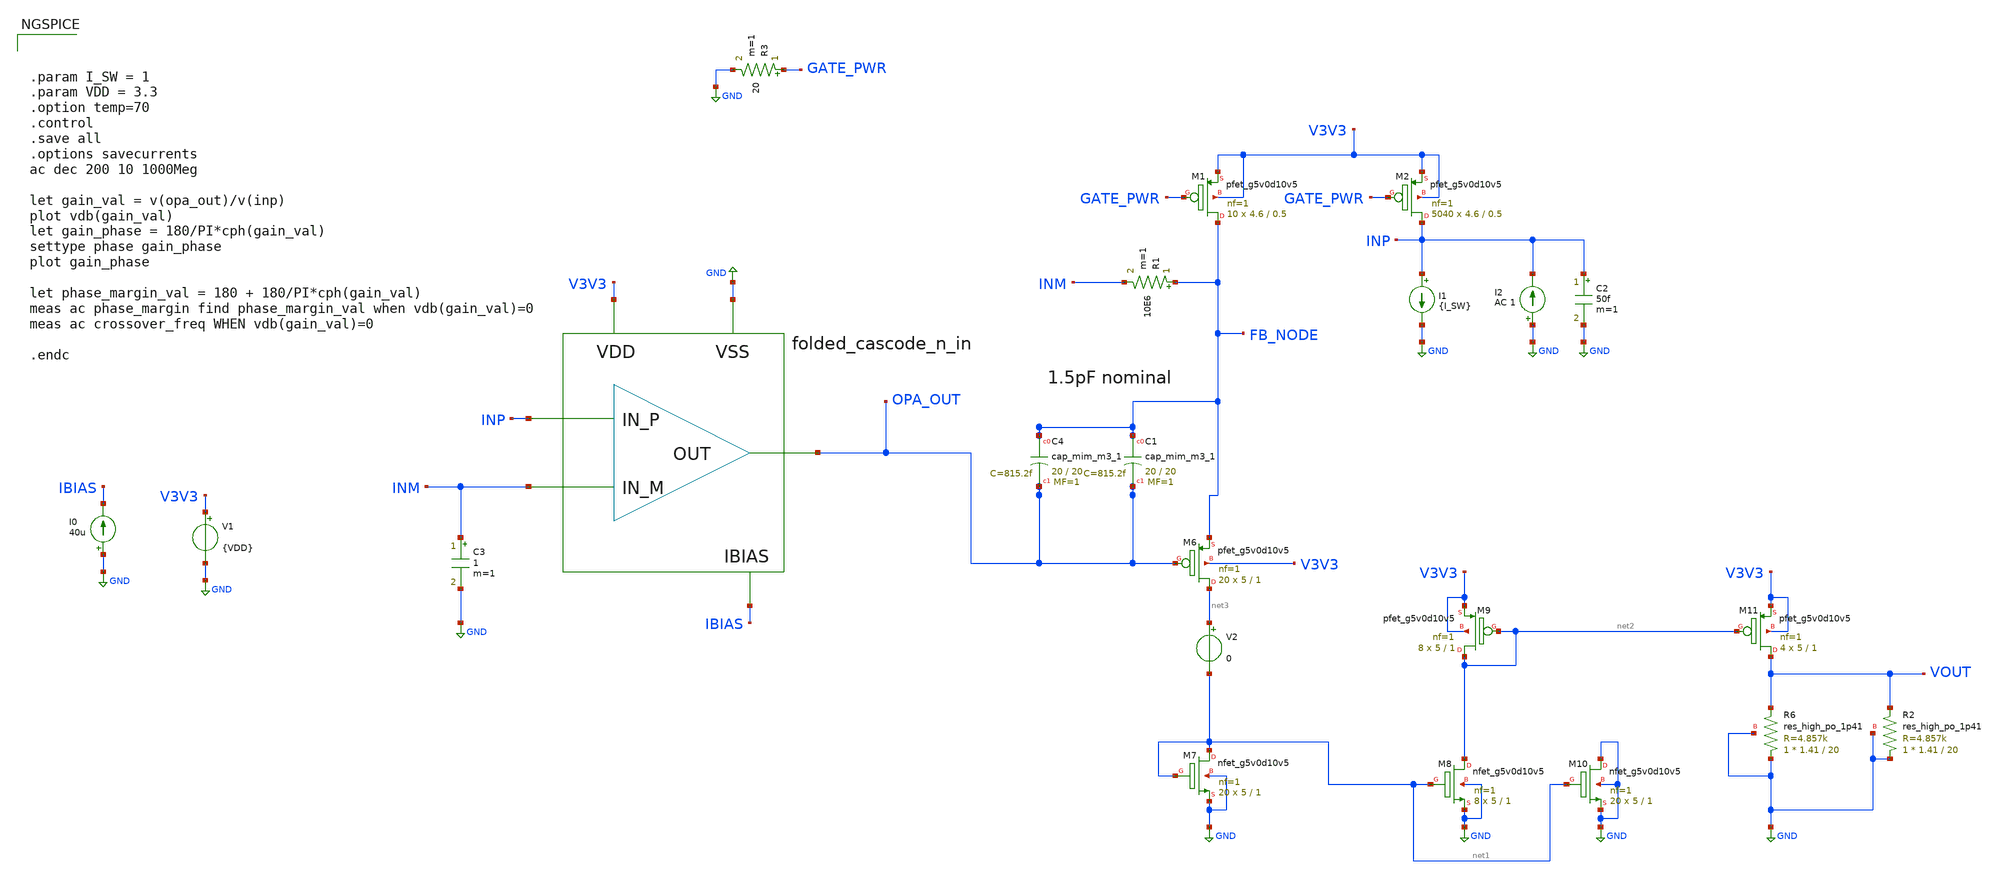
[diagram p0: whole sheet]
** sch_path: images/foss-asic-tools/addons/examples/open-pmic/design/current-sense/current_sense_ac_phase_margin.sch
**.subckt current_sense_ac_phase_margin
V1 V3V3 GND {VDD}
I0 GND IBIAS 40u
x1 INP INM OPA_OUT V3V3 GND IBIAS folded_cascode_n_in
XM1 FB_NODE GATE_PWR V3V3 V3V3 sky130_fd_pr__pfet_g5v0d10v5 L=0.5 W=4.6 nf=1 ad='int((nf+1)/2) * W/nf * 0.29'
+ as='int((nf+2)/2) * W/nf * 0.29' pd='2*int((nf+1)/2) * (W/nf + 0.29)' ps='2*int((nf+2)/2) * (W/nf + 0.29)'
+ nrd='0.29 / W' nrs='0.29 / W' sa=0 sb=0 sd=0 mult=10 m=10
XM2 INP GATE_PWR V3V3 V3V3 sky130_fd_pr__pfet_g5v0d10v5 L=0.5 W=4.6 nf=1 ad='int((nf+1)/2) * W/nf * 0.29'
+ as='int((nf+2)/2) * W/nf * 0.29' pd='2*int((nf+1)/2) * (W/nf + 0.29)' ps='2*int((nf+2)/2) * (W/nf + 0.29)'
+ nrd='0.29 / W' nrs='0.29 / W' sa=0 sb=0 sd=0 mult=5040 m=5040
R3 GATE_PWR GND 20 m=1
I1 INP GND {I_SW}
I2 GND INP AC 1
C2 INP GND 50f m=1
XM6 net3 OPA_OUT FB_NODE V3V3 sky130_fd_pr__pfet_g5v0d10v5 L=1 W=5 nf=1 ad='int((nf+1)/2) * W/nf * 0.29'
+ as='int((nf+2)/2) * W/nf * 0.29' pd='2*int((nf+1)/2) * (W/nf + 0.29)' ps='2*int((nf+2)/2) * (W/nf + 0.29)'
+ nrd='0.29 / W' nrs='0.29 / W' sa=0 sb=0 sd=0 mult=20 m=20
XM7 net1 net1 GND GND sky130_fd_pr__nfet_g5v0d10v5 L=1 W=5 nf=1 ad='int((nf+1)/2) * W/nf * 0.29' as='int((nf+2)/2) * W/nf * 0.29'
+ pd='2*int((nf+1)/2) * (W/nf + 0.29)' ps='2*int((nf+2)/2) * (W/nf + 0.29)' nrd='0.29 / W' nrs='0.29 / W'
+ sa=0 sb=0 sd=0 mult=20 m=20
XM8 net2 net1 GND GND sky130_fd_pr__nfet_g5v0d10v5 L=1 W=5 nf=1 ad='int((nf+1)/2) * W/nf * 0.29' as='int((nf+2)/2) * W/nf * 0.29'
+ pd='2*int((nf+1)/2) * (W/nf + 0.29)' ps='2*int((nf+2)/2) * (W/nf + 0.29)' nrd='0.29 / W' nrs='0.29 / W'
+ sa=0 sb=0 sd=0 mult=8 m=8
XM9 net2 net2 V3V3 V3V3 sky130_fd_pr__pfet_g5v0d10v5 L=1 W=5 nf=1 ad='int((nf+1)/2) * W/nf * 0.29' as='int((nf+2)/2) * W/nf * 0.29'
+ pd='2*int((nf+1)/2) * (W/nf + 0.29)' ps='2*int((nf+2)/2) * (W/nf + 0.29)' nrd='0.29 / W' nrs='0.29 / W'
+ sa=0 sb=0 sd=0 mult=8 m=8
XM10 GND net1 GND GND sky130_fd_pr__nfet_g5v0d10v5 L=1 W=5 nf=1 ad='int((nf+1)/2) * W/nf * 0.29' as='int((nf+2)/2) * W/nf * 0.29'
+ pd='2*int((nf+1)/2) * (W/nf + 0.29)' ps='2*int((nf+2)/2) * (W/nf + 0.29)' nrd='0.29 / W' nrs='0.29 / W'
+ sa=0 sb=0 sd=0 mult=20 m=20
XM11 VOUT net2 V3V3 V3V3 sky130_fd_pr__pfet_g5v0d10v5 L=1 W=5 nf=1 ad='int((nf+1)/2) * W/nf * 0.29' as='int((nf+2)/2) * W/nf * 0.29'
+ pd='2*int((nf+1)/2) * (W/nf + 0.29)' ps='2*int((nf+2)/2) * (W/nf + 0.29)' nrd='0.29 / W' nrs='0.29 / W'
+ sa=0 sb=0 sd=0 mult=4 m=4
XR6 GND VOUT GND sky130_fd_pr__res_high_po_1p41 L=20 mult=1 m=1
XR2 GND VOUT GND sky130_fd_pr__res_high_po_1p41 L=20 mult=1 m=1
V2 net3 net1 0
XC4 FB_NODE OPA_OUT sky130_fd_pr__cap_mim_m3_1 W=20 L=20 MF=1 m=1
XC1 FB_NODE OPA_OUT sky130_fd_pr__cap_mim_m3_1 W=20 L=20 MF=1 m=1
R1 FB_NODE INM 10E6 m=1
C3 INM GND 1 m=1
**** begin user architecture code



.param I_SW = 1
.param VDD = 3.3
.option temp=70
.control
.save all
.options savecurrents
ac dec 200 10 1000Meg

let gain_val = v(opa_out)/v(inp)
plot vdb(gain_val)
let gain_phase = 180/PI*cph(gain_val)
settype phase gain_phase
plot gain_phase

let phase_margin_val = 180 + 180/PI*cph(gain_val)
meas ac phase_margin find phase_margin_val when vdb(gain_val)=0
meas ac crossover_freq WHEN vdb(gain_val)=0

.endc



.lib $::SKYWATER_MODELS/models/sky130.lib.spice tt
.option wnflag=1

**** end user architecture code
**.ends
.GLOBAL GND
**** begin user architecture code
[sky130_models]
**** end user architecture code
.end
